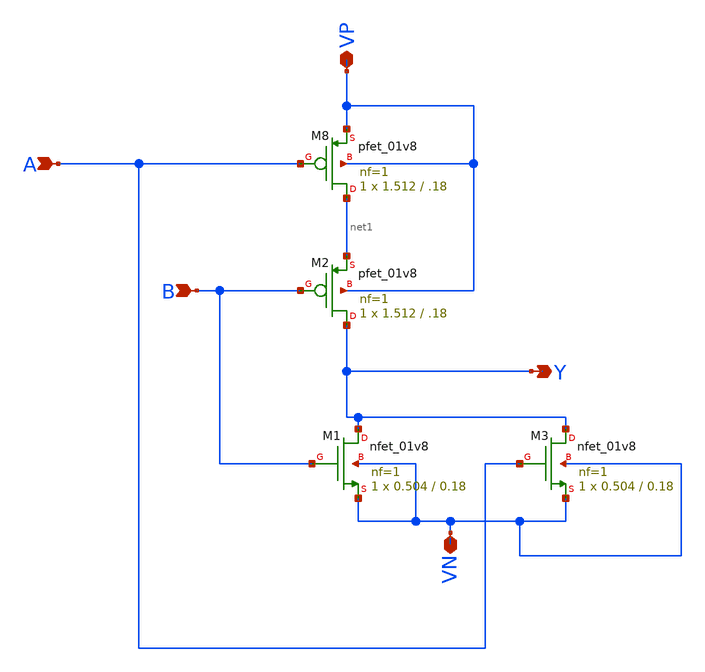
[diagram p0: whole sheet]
** sch_path: component/OR_gate/ORG.sch
**.subckt ORG A B Y VP VN
*.ipin A
*.ipin B
*.opin Y
*.iopin VP
*.iopin VN
XM3 Y A VN VN sky130_fd_pr__nfet_01v8 L=0.18 W=0.504 nf=1 ad='int((nf+1)/2) * W/nf * 0.29' as='int((nf+2)/2) * W/nf * 0.29'
+ pd='2*int((nf+1)/2) * (W/nf + 0.29)' ps='2*int((nf+2)/2) * (W/nf + 0.29)' nrd='0.29 / W' nrs='0.29 / W'
+ sa=0 sb=0 sd=0 mult=1 m=1
XM8 net1 A VP VP sky130_fd_pr__pfet_01v8 L=.18 W=1.512 nf=1 ad='int((nf+1)/2) * W/nf * 0.29' as='int((nf+2)/2) * W/nf * 0.29'
+ pd='2*int((nf+1)/2) * (W/nf + 0.29)' ps='2*int((nf+2)/2) * (W/nf + 0.29)' nrd='0.29 / W' nrs='0.29 / W'
+ sa=0 sb=0 sd=0 mult=1 m=1
XM2 Y B net1 VP sky130_fd_pr__pfet_01v8 L=.18 W=1.512 nf=1 ad='int((nf+1)/2) * W/nf * 0.29' as='int((nf+2)/2) * W/nf * 0.29'
+ pd='2*int((nf+1)/2) * (W/nf + 0.29)' ps='2*int((nf+2)/2) * (W/nf + 0.29)' nrd='0.29 / W' nrs='0.29 / W'
+ sa=0 sb=0 sd=0 mult=1 m=1
XM1 Y B VN VN sky130_fd_pr__nfet_01v8 L=0.18 W=0.504 nf=1 ad='int((nf+1)/2) * W/nf * 0.29' as='int((nf+2)/2) * W/nf * 0.29'
+ pd='2*int((nf+1)/2) * (W/nf + 0.29)' ps='2*int((nf+2)/2) * (W/nf + 0.29)' nrd='0.29 / W' nrs='0.29 / W'
+ sa=0 sb=0 sd=0 mult=1 m=1
**.ends
.end
